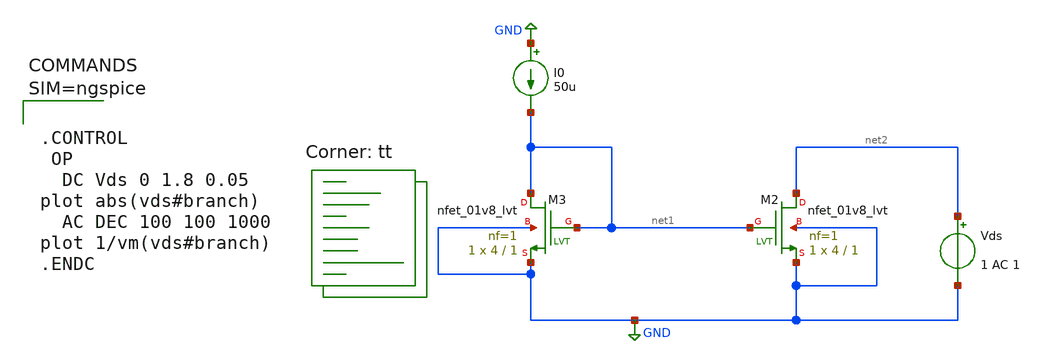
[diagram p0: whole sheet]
** sch_path: Work/xschem/currentmirror_1_nmos.sch
**.subckt currentmirror_1_nmos
XM2 net2 net1 GND GND sky130_fd_pr__nfet_01v8_lvt L=1 W=4 nf=1 ad='int((1 + 1)/2) * 4 / 1 * 0.29' as='int((1 + 2)/2) * 4 / 1 * 0.29'
+ pd='2*int((1 + 1)/2) * (4 / 1 + 0.29)' ps='2*int((1 + 2)/2) * (4 / 1 + 0.29)' nrd='0.29 / 4 ' nrs='0.29 / 4 '
+ sa=0 sb=0 sd=0 mult=1 m=1
I0 GND net1 50u
Vds net2 GND 1 AC 1
XM3 net1 net1 GND GND sky130_fd_pr__nfet_01v8_lvt L=1 W=4 nf=1 ad='int((1 + 1)/2) * 4 / 1 * 0.29' as='int((1 + 2)/2) * 4 / 1 * 0.29'
+ pd='2*int((1 + 1)/2) * (4 / 1 + 0.29)' ps='2*int((1 + 2)/2) * (4 / 1 + 0.29)' nrd='0.29 / 4 ' nrs='0.29 / 4 '
+ sa=0 sb=0 sd=0 mult=1 m=1
**** begin user architecture code



.CONTROL
 OP
  DC Vds 0 1.8 0.05
plot abs(vds#branch)
  AC DEC 100 100 1000
plot 1/vm(vds#branch)
.ENDC



.lib $::SKYWATER_MODELS/sky130.lib.spice tt
.lib /usr/local/share/pdk/sky130A/libs.tech/ngspice/sky130.lib.spice tt
**** end user architecture code
**.ends
.GLOBAL GND
.end
